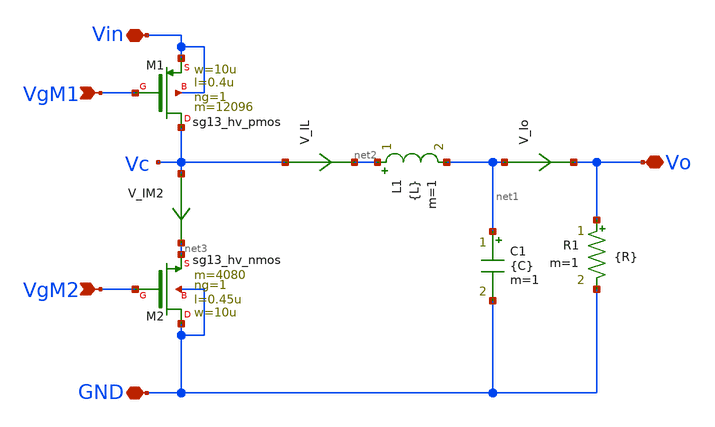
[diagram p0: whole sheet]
** sch_path: xschem/DCDCBuck/DCDCBuck_vto1p1.sch
**.subckt DCDCBuck_vto1p1 Vin VgM1 VgM2 Vo GND
*.iopin Vin
*.ipin VgM1
*.ipin VgM2
*.iopin Vo
*.iopin GND
XM2 GND VgM2 net3 GND sg13_hv_nmos w=10u l=0.45u ng=1 m=4080 mm_ok=1
XM1 Vc VgM1 Vin Vin sg13_hv_pmos w=10u l=0.4u ng=1 m=12096 mm_ok=1
L1 net2 net1 {L} m=1
C1 net1 GND {C} m=1
V_Io net1 Vo 0
.save i(v_io)
V_IL Vc net2 0
.save i(v_il)
R1 Vo GND {R} m=1
V_IM2 Vc net3 0
.save i(v_im2)
**.ends
.end
